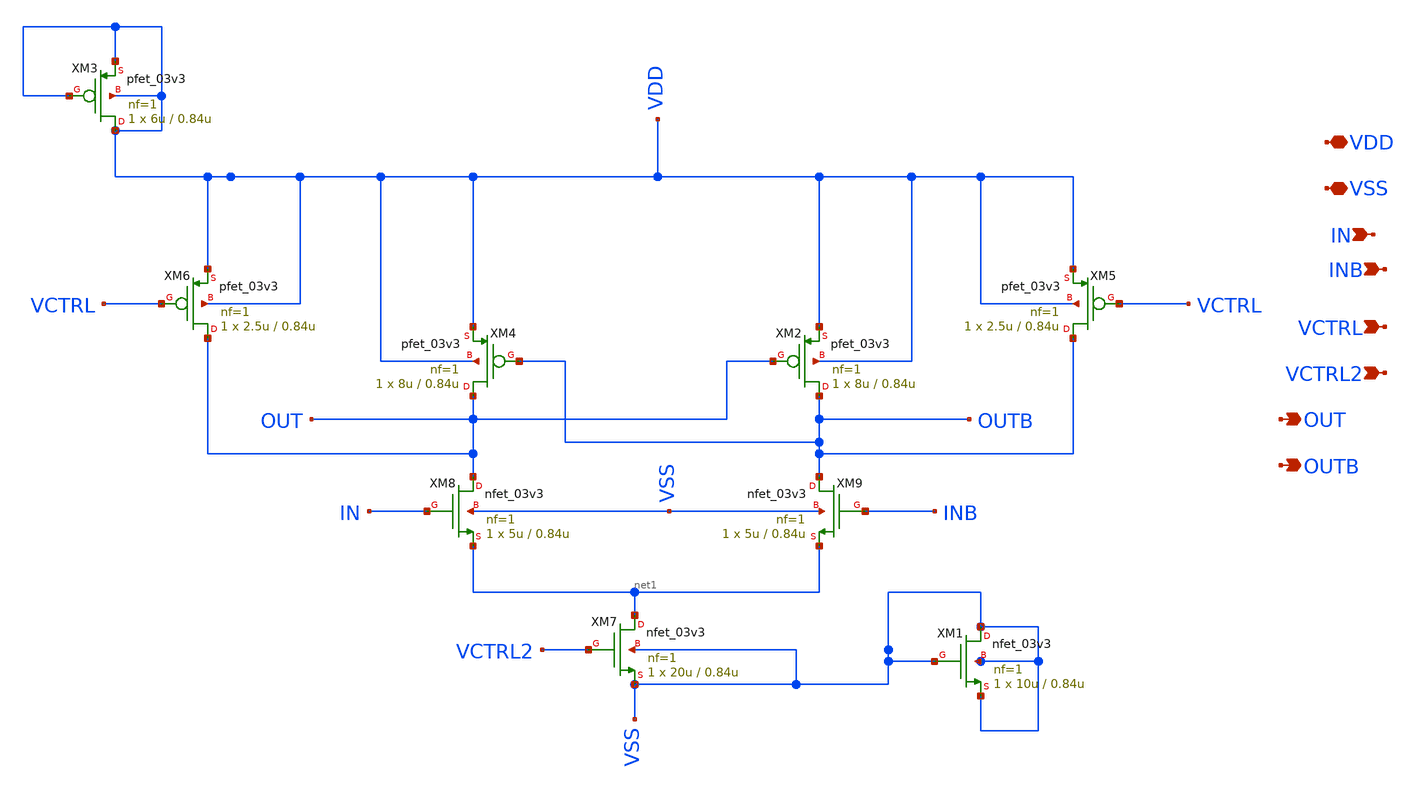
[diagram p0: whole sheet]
** sch_path: PLL-main/schematic/xschem/DelayCell_1.sch
**.subckt DelayCell_1 VDD VSS IN INB VCTRL VCTRL2 OUT OUTB
*.iopin VDD
*.iopin VSS
*.ipin IN
*.ipin INB
*.ipin VCTRL
*.ipin VCTRL2
*.opin OUT
*.opin OUTB
XM2 OUTB OUT VDD VDD pfet_03v3 L=0.84u W=8u nf=1 ad='int((nf+1)/2) * W/nf * 0.18u' as='int((nf+2)/2) * W/nf * 0.18u'
+ pd='2*int((nf+1)/2) * (W/nf + 0.18u)' ps='2*int((nf+2)/2) * (W/nf + 0.18u)' nrd='0.18u / W' nrs='0.18u / W'
+ sa=0 sb=0 sd=0 m=1
XM4 OUT OUTB VDD VDD pfet_03v3 L=0.84u W=8u nf=1 ad='int((nf+1)/2) * W/nf * 0.18u' as='int((nf+2)/2) * W/nf * 0.18u'
+ pd='2*int((nf+1)/2) * (W/nf + 0.18u)' ps='2*int((nf+2)/2) * (W/nf + 0.18u)' nrd='0.18u / W' nrs='0.18u / W'
+ sa=0 sb=0 sd=0 m=1
XM5 OUTB VCTRL VDD VDD pfet_03v3 L=0.84u W=2.5u nf=1 ad='int((nf+1)/2) * W/nf * 0.18u' as='int((nf+2)/2) * W/nf * 0.18u'
+ pd='2*int((nf+1)/2) * (W/nf + 0.18u)' ps='2*int((nf+2)/2) * (W/nf + 0.18u)' nrd='0.18u / W' nrs='0.18u / W'
+ sa=0 sb=0 sd=0 m=1
XM6 OUT VCTRL VDD VDD pfet_03v3 L=0.84u W=2.5u nf=1 ad='int((nf+1)/2) * W/nf * 0.18u' as='int((nf+2)/2) * W/nf * 0.18u'
+ pd='2*int((nf+1)/2) * (W/nf + 0.18u)' ps='2*int((nf+2)/2) * (W/nf + 0.18u)' nrd='0.18u / W' nrs='0.18u / W'
+ sa=0 sb=0 sd=0 m=1
XM7 net1 VCTRL2 VSS VSS nfet_03v3 L=0.84u W=20u nf=1 ad='int((nf+1)/2) * W/nf * 0.18u' as='int((nf+2)/2) * W/nf * 0.18u'
+ pd='2*int((nf+1)/2) * (W/nf + 0.18u)' ps='2*int((nf+2)/2) * (W/nf + 0.18u)' nrd='0.18u / W' nrs='0.18u / W'
+ sa=0 sb=0 sd=0 m=1
XM8 OUT IN net1 VSS nfet_03v3 L=0.84u W=5u nf=1 ad='int((nf+1)/2) * W/nf * 0.18u' as='int((nf+2)/2) * W/nf * 0.18u'
+ pd='2*int((nf+1)/2) * (W/nf + 0.18u)' ps='2*int((nf+2)/2) * (W/nf + 0.18u)' nrd='0.18u / W' nrs='0.18u / W'
+ sa=0 sb=0 sd=0 m=1
XM9 OUTB INB net1 VSS nfet_03v3 L=0.84u W=5u nf=1 ad='int((nf+1)/2) * W/nf * 0.18u' as='int((nf+2)/2) * W/nf * 0.18u'
+ pd='2*int((nf+1)/2) * (W/nf + 0.18u)' ps='2*int((nf+2)/2) * (W/nf + 0.18u)' nrd='0.18u / W' nrs='0.18u / W'
+ sa=0 sb=0 sd=0 m=1
XM1 VSS VSS VSS VSS nfet_03v3 L=0.84u W=10u nf=1 ad='int((nf+1)/2) * W/nf * 0.18u' as='int((nf+2)/2) * W/nf * 0.18u'
+ pd='2*int((nf+1)/2) * (W/nf + 0.18u)' ps='2*int((nf+2)/2) * (W/nf + 0.18u)' nrd='0.18u / W' nrs='0.18u / W'
+ sa=0 sb=0 sd=0 m=1
XM3 VDD VDD VDD VDD pfet_03v3 L=0.84u W=6u nf=1 ad='int((nf+1)/2) * W/nf * 0.18u' as='int((nf+2)/2) * W/nf * 0.18u'
+ pd='2*int((nf+1)/2) * (W/nf + 0.18u)' ps='2*int((nf+2)/2) * (W/nf + 0.18u)' nrd='0.18u / W' nrs='0.18u / W'
+ sa=0 sb=0 sd=0 m=1
**.ends
.end
